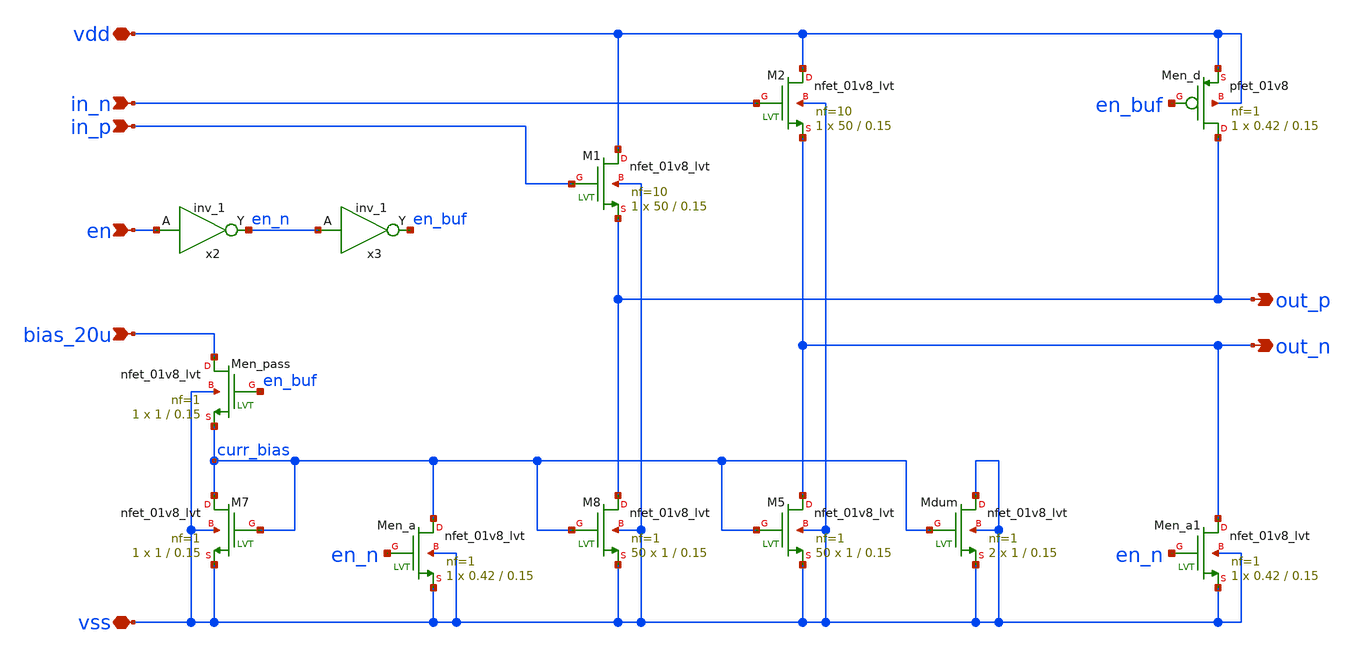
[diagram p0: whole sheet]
** sch_path: design/lc_oscillator_buffer/lc_oscillator_buffer.sch
**.subckt lc_oscillator_buffer vss vdd out_p out_n bias_20u in_p in_n en
*.iopin vss
*.iopin vdd
*.opin out_p
*.opin out_n
*.ipin bias_20u
*.ipin in_p
*.ipin in_n
*.ipin en
XM1 vdd in_p out_p vss sky130_fd_pr__nfet_01v8_lvt L=0.15 W=50 nf=10 ad='int((nf+1)/2) * W/nf * 0.29'
+ as='int((nf+2)/2) * W/nf * 0.29' pd='2*int((nf+1)/2) * (W/nf + 0.29)' ps='2*int((nf+2)/2) * (W/nf + 0.29)'
+ nrd='0.29 / W' nrs='0.29 / W' sa=0 sb=0 sd=0 mult=1 m=1
XM2 vdd in_n out_n vss sky130_fd_pr__nfet_01v8_lvt L=0.15 W=50 nf=10 ad='int((nf+1)/2) * W/nf * 0.29'
+ as='int((nf+2)/2) * W/nf * 0.29' pd='2*int((nf+1)/2) * (W/nf + 0.29)' ps='2*int((nf+2)/2) * (W/nf + 0.29)'
+ nrd='0.29 / W' nrs='0.29 / W' sa=0 sb=0 sd=0 mult=1 m=1
XM5 out_n curr_bias vss vss sky130_fd_pr__nfet_01v8_lvt L=0.15 W=1 nf=1 ad='int((nf+1)/2) * W/nf * 0.29'
+ as='int((nf+2)/2) * W/nf * 0.29' pd='2*int((nf+1)/2) * (W/nf + 0.29)' ps='2*int((nf+2)/2) * (W/nf + 0.29)'
+ nrd='0.29 / W' nrs='0.29 / W' sa=0 sb=0 sd=0 mult=50 m=50
XM7 curr_bias curr_bias vss vss sky130_fd_pr__nfet_01v8_lvt L=0.15 W=1 nf=1 ad='int((nf+1)/2) * W/nf * 0.29'
+ as='int((nf+2)/2) * W/nf * 0.29' pd='2*int((nf+1)/2) * (W/nf + 0.29)' ps='2*int((nf+2)/2) * (W/nf + 0.29)'
+ nrd='0.29 / W' nrs='0.29 / W' sa=0 sb=0 sd=0 mult=1 m=1
XM8 out_p curr_bias vss vss sky130_fd_pr__nfet_01v8_lvt L=0.15 W=1 nf=1 ad='int((nf+1)/2) * W/nf * 0.29'
+ as='int((nf+2)/2) * W/nf * 0.29' pd='2*int((nf+1)/2) * (W/nf + 0.29)' ps='2*int((nf+2)/2) * (W/nf + 0.29)'
+ nrd='0.29 / W' nrs='0.29 / W' sa=0 sb=0 sd=0 mult=50 m=50
x2 en vss vss vdd vdd en_n sky130_fd_sc_hs__inv_1
x3 en_n vss vss vdd vdd en_buf sky130_fd_sc_hs__inv_1
XMen_pass bias_20u en_buf curr_bias vss sky130_fd_pr__nfet_01v8_lvt L=0.15 W=1 nf=1 ad='int((nf+1)/2) * W/nf * 0.29'
+ as='int((nf+2)/2) * W/nf * 0.29' pd='2*int((nf+1)/2) * (W/nf + 0.29)' ps='2*int((nf+2)/2) * (W/nf + 0.29)'
+ nrd='0.29 / W' nrs='0.29 / W' sa=0 sb=0 sd=0 mult=1 m=1
XMen_a curr_bias en_n vss vss sky130_fd_pr__nfet_01v8_lvt L=0.15 W=0.42 nf=1 ad='int((nf+1)/2) * W/nf * 0.29'
+ as='int((nf+2)/2) * W/nf * 0.29' pd='2*int((nf+1)/2) * (W/nf + 0.29)' ps='2*int((nf+2)/2) * (W/nf + 0.29)'
+ nrd='0.29 / W' nrs='0.29 / W' sa=0 sb=0 sd=0 mult=1 m=1
XMen_a1 out_n en_n vss vss sky130_fd_pr__nfet_01v8_lvt L=0.15 W=0.42 nf=1 ad='int((nf+1)/2) * W/nf * 0.29'
+ as='int((nf+2)/2) * W/nf * 0.29' pd='2*int((nf+1)/2) * (W/nf + 0.29)' ps='2*int((nf+2)/2) * (W/nf + 0.29)'
+ nrd='0.29 / W' nrs='0.29 / W' sa=0 sb=0 sd=0 mult=1 m=1
XMen_d out_p en_buf vdd vdd sky130_fd_pr__pfet_01v8 L=0.15 W=0.42 nf=1 ad='int((nf+1)/2) * W/nf * 0.29'
+ as='int((nf+2)/2) * W/nf * 0.29' pd='2*int((nf+1)/2) * (W/nf + 0.29)' ps='2*int((nf+2)/2) * (W/nf + 0.29)'
+ nrd='0.29 / W' nrs='0.29 / W' sa=0 sb=0 sd=0 mult=1 m=1
XMdum vss curr_bias vss vss sky130_fd_pr__nfet_01v8_lvt L=0.15 W=1 nf=1 ad='int((nf+1)/2) * W/nf * 0.29'
+ as='int((nf+2)/2) * W/nf * 0.29' pd='2*int((nf+1)/2) * (W/nf + 0.29)' ps='2*int((nf+2)/2) * (W/nf + 0.29)'
+ nrd='0.29 / W' nrs='0.29 / W' sa=0 sb=0 sd=0 mult=2 m=2
**.ends
.end
